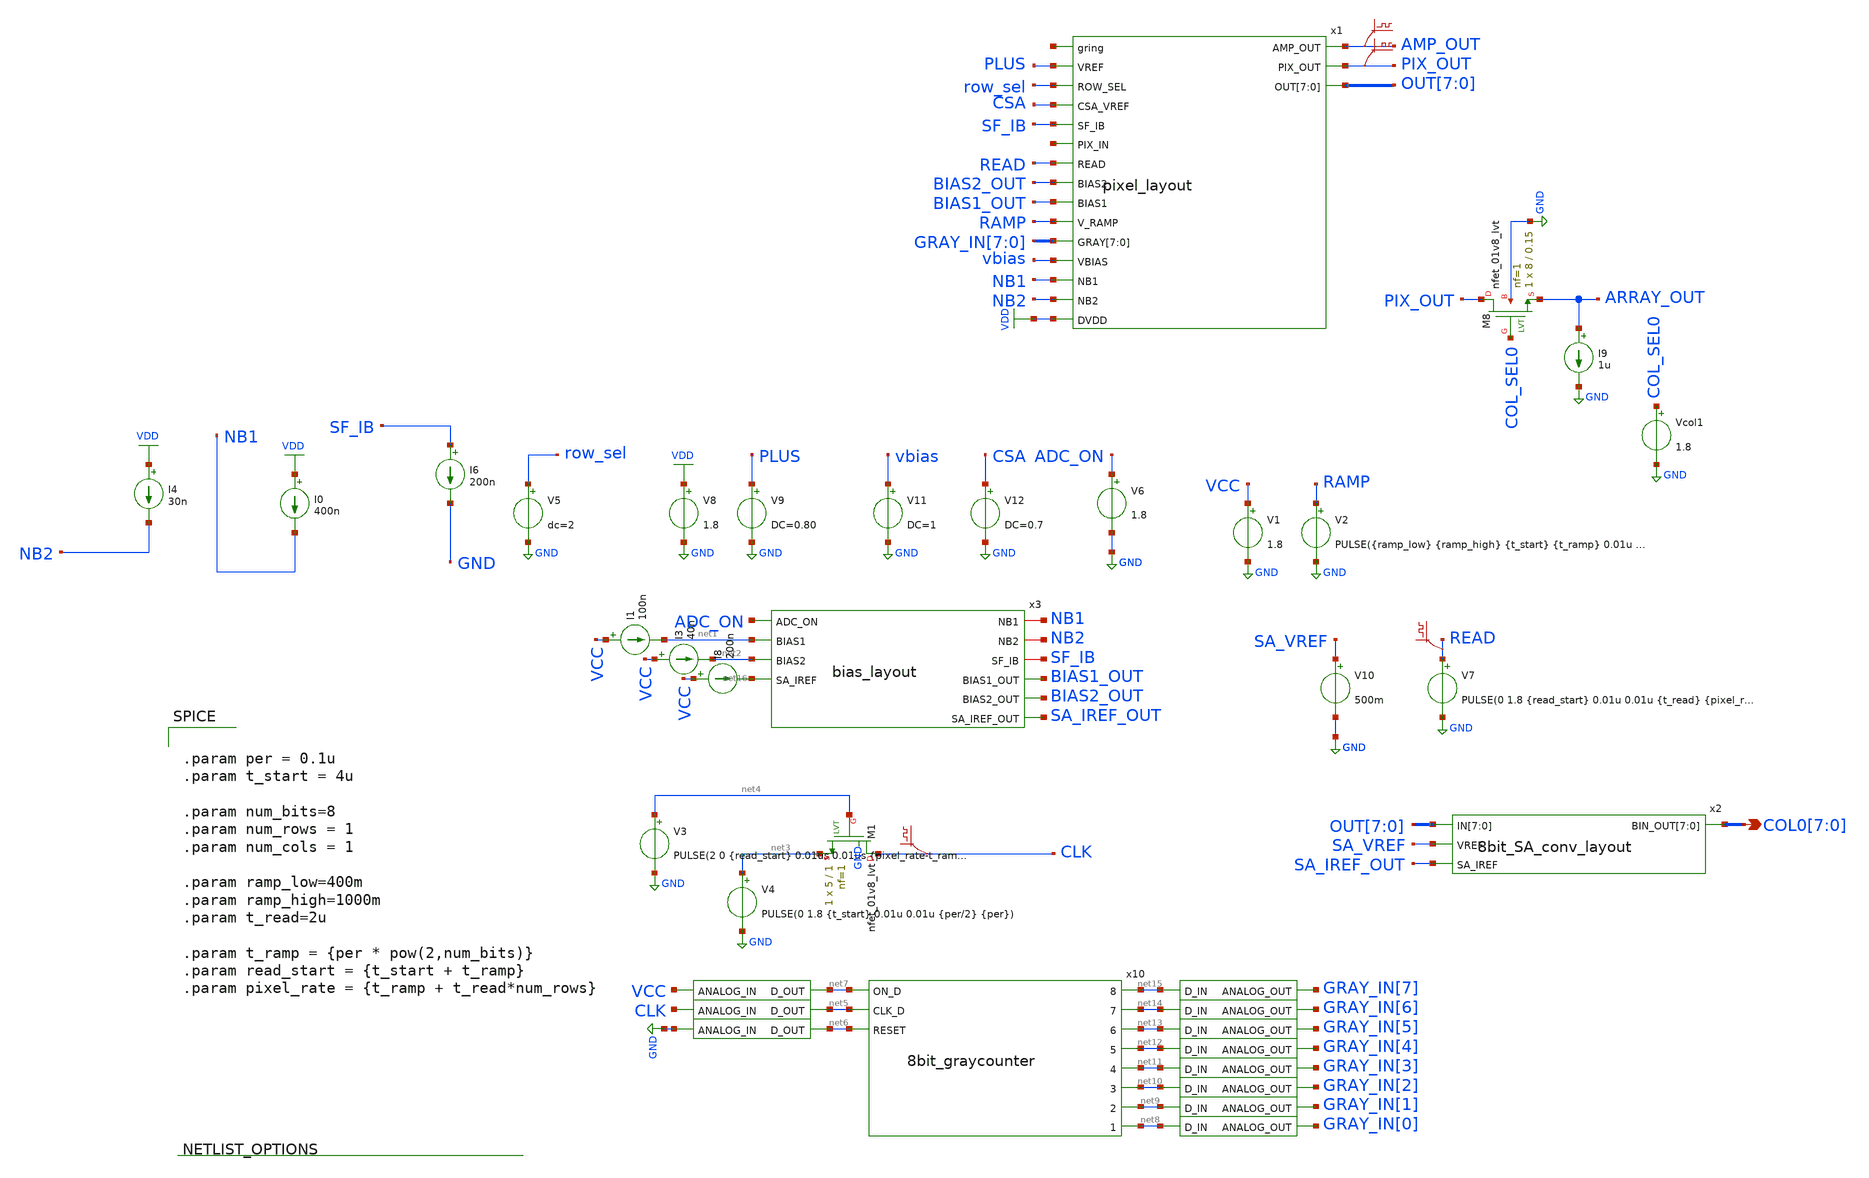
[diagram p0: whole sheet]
** sch_path: xschem/testbench/pixel_components_tb.sch
**.subckt pixel_components_tb COL0[7],COL0[6],COL0[5],COL0[4],COL0[3],COL0[2],COL0[1],COL0[0]
*.opin COL0[7],COL0[6],COL0[5],COL0[4],COL0[3],COL0[2],COL0[1],COL0[0]
V8 VDD GND 1.8
V9 PLUS GND DC=0.80
V11 vbias GND DC=1
V12 CSA GND DC=0.7
I1 VCC net1 100n
I3 VCC net2 40n
I8 VCC net16 200n
V6 ADC_ON GND 1.8
I4 VDD NB2 30n
I6 SF_IB GND 200n
V5 row_sel GND dc=2
I0 VDD NB1 400n
V1 VCC GND 1.8
V2 RAMP GND PULSE({ramp_low} {ramp_high} {t_start} {t_ramp} 0.01u {pixel_rate-t_ramp} {pixel_rate})
V10 SA_VREF GND 500m
V4 net3 GND PULSE(0 1.8 {t_start} 0.01u 0.01u {per/2} {per})
V3 net4 GND PULSE(2 0 {read_start} 0.01us 0.01us {pixel_rate-t_ramp} {pixel_rate})
.save v(clk)
XM1 CLK net4 net3 GND sky130_fd_pr__nfet_01v8_lvt L=1 W=5 nf=1 ad='int((nf+1)/2) * W/nf * 0.29' as='int((nf+2)/2) * W/nf * 0.29'
+ pd='2*int((nf+1)/2) * (W/nf + 0.29)' ps='2*int((nf+2)/2) * (W/nf + 0.29)' nrd='0.29 / W' nrs='0.29 / W'
+ sa=0 sb=0 sd=0 mult=1 m=1
x6 net6 GND adc_bridge
x8 net7 VCC adc_bridge
x7 net5 CLK adc_bridge
x10 net15 net7 net14 net5 net13 net12 net6 net11 net10 net9 net8 8bit_graycounter
x5 GRAY_IN[7] net15 dac_bridge
x9 GRAY_IN[6] net14 dac_bridge
x11 GRAY_IN[5] net13 dac_bridge
x12 GRAY_IN[4] net12 dac_bridge
x13 GRAY_IN[3] net11 dac_bridge
x14 GRAY_IN[2] net10 dac_bridge
x15 GRAY_IN[1] net9 dac_bridge
x16 GRAY_IN[0] net8 dac_bridge
V7 READ GND PULSE(0 1.8 {read_start} 0.01u 0.01u {t_read} {pixel_rate})
.save v(read)
.save v(amp_out)
.save v(pix_out)
XM8 PIX_OUT COL_SEL0 ARRAY_OUT GND sky130_fd_pr__nfet_01v8_lvt L=0.15 W=8 nf=1 ad='int((nf+1)/2) * W/nf * 0.29'
+ as='int((nf+2)/2) * W/nf * 0.29' pd='2*int((nf+1)/2) * (W/nf + 0.29)' ps='2*int((nf+2)/2) * (W/nf + 0.29)'
+ nrd='0.29 / W' nrs='0.29 / W' sa=0 sb=0 sd=0 mult=1 m=1
I9 ARRAY_OUT GND 1u
Vcol1 COL_SEL0 GND 1.8
x1 AMP_OUT net17 PLUS row_sel PIX_OUT CSA OUT[7] OUT[6] OUT[5] OUT[4] OUT[3] OUT[2] OUT[1] OUT[0]
+ SF_IB net18 READ BIAS2_OUT BIAS1_OUT RAMP GRAY_IN[7] GRAY_IN[6] GRAY_IN[5] GRAY_IN[4] GRAY_IN[3]
+ GRAY_IN[2] GRAY_IN[1] GRAY_IN[0] vbias NB1 NB2 VDD pixel_layout
x3 NB1 NB2 SF_IB ADC_ON net1 BIAS1_OUT BIAS2_OUT net2 SA_IREF_OUT net16 bias_layout
x2 OUT[7] OUT[6] OUT[5] OUT[4] OUT[3] OUT[2] OUT[1] OUT[0] SA_VREF SA_IREF_OUT COL0[7] COL0[6]
+ COL0[5] COL0[4] COL0[3] COL0[2] COL0[1] COL0[0] 8bit_SA_conv_layout
**** begin user architecture code

** opencircuitdesign pdks install
.lib $::SKYWATER_MODELS/sky130.lib.spice tt
.global vcc



.param per = 0.1u
.param t_start = 4u

.param num_bits=8
.param num_rows = 1
.param num_cols = 1

.param ramp_low=400m
.param ramp_high=1000m
.param t_read=2u

.param t_ramp = {per * pow(2,num_bits)}
.param read_start = {t_start + t_ramp}
.param pixel_rate = {t_ramp + t_read*num_rows}


**** end user architecture code
**.ends

* expanding   symbol:  digital_prims/adc_bridge.sym # of pins=2
** sym_path: xschem/digital_prims/adc_bridge.sym
** sch_path: xschem/digital_prims/adc_bridge.sch
.subckt adc_bridge D_OUT ANALOG_IN
*.ipin ANALOG_IN
*.opin D_OUT
**** begin user architecture code


abridge [ANALOG_IN] [D_OUT] adc_buff
.model adc_buff adc_bridge(in_low=0.9 in_high =0.9)


**** end user architecture code
.ends


* expanding   symbol:  adc/8bit_graycounter.sym # of pins=11
** sym_path: xschem/adc/8bit_graycounter.sym
** sch_path: xschem/adc/8bit_graycounter.sch
.subckt 8bit_graycounter 8 ON_D 7 CLK_D 6 5 RESET 4 3 2 1
*.ipin ON_D
*.ipin CLK_D
*.ipin RESET
*.opin 7
*.opin 6
*.opin 5
*.opin 4
*.opin 3
*.opin 2
*.opin 1
*.opin 8
**** begin user architecture code


a1 [ON_D] CLK_D RESET [8 7 6 5 4 3 2 1] gc_sm
.model gc_sm d_state(state_file="/home/hni/topmetal_dps/xschem/adc/graycntr.in")


**** end user architecture code
.ends


* expanding   symbol:  digital_prims/dac_bridge.sym # of pins=2
** sym_path: xschem/digital_prims/dac_bridge.sym
** sch_path: xschem/digital_prims/dac_bridge.sch
.subckt dac_bridge ANALOG_OUT D_IN
*.ipin D_IN
*.opin ANALOG_OUT
**** begin user architecture code


abridge_d [D_IN] [ANALOG_OUT] dac_buff
.model dac_buff dac_bridge(out_high=1.8)


**** end user architecture code
.ends


* expanding   symbol:  post_layout/pixel_layout.sym # of pins=18
** sym_path: xschem/post_layout/pixel_layout.sym
** sch_path: xschem/post_layout/pixel_layout.sch
.subckt pixel_layout AMP_OUT gring VREF ROW_SEL PIX_OUT CSA_VREF OUT[7] OUT[6] OUT[5] OUT[4] OUT[3]
+ OUT[2] OUT[1] OUT[0] SF_IB PIX_IN READ BIAS2 BIAS1 V_RAMP GRAY[7] GRAY[6] GRAY[5] GRAY[4] GRAY[3] GRAY[2]
+ GRAY[1] GRAY[0] VBIAS NB1 NB2 DVDD
*.opin AMP_OUT
*.ipin gring
*.ipin VREF
*.ipin ROW_SEL
*.opin PIX_OUT
*.ipin CSA_VREF
*.ipin SF_IB
*.ipin PIX_IN
*.ipin READ
*.ipin BIAS2
*.ipin BIAS1
*.ipin V_RAMP
*.ipin GRAY[7],GRAY[6],GRAY[5],GRAY[4],GRAY[3],GRAY[2],GRAY[1],GRAY[0]
*.ipin VBIAS
*.ipin NB1
*.ipin NB2
*.ipin DVDD
*.opin OUT[7],OUT[6],OUT[5],OUT[4],OUT[3],OUT[2],OUT[1],OUT[0]
**** begin user architecture code


X8bit_dram_0 READ GRAYx2x OUTx4x OUTx2x OUTx6x GRAYx3x GRAYx4x OUTx0x GRAYx1x OUTx7x  GRAYx5x OUTx3x
+ GRAYx7x 8bit_dram_0/4bit_dram_1/dram_array_1/dram_cell_1/WWL OUTx5x  OUTx1x GRAYx6x GND GRAYx0x x8bit_dram
X0 a_2200_n380# ROW_SEL PIX_OUT GND sky130_fd_pr__nfet_01v8_lvt ad=6.5e+11p pd=5e+06u as=1e+12p
+ ps=5e+06u w=2e+06u l=1e+06u
X1 DVDD a_1000_n1450# a_1000_n1450# DVDD sky130_fd_pr__pfet_01v8_lvt ad=1.45e+12p pd=1.09e+07u
+ as=3.5e+11p ps=2.7e+06u w=1e+06u l=1e+06u
X2 8bit_dram_0/4bit_dram_1/dram_array_1/dram_cell_1/WWL a_1870_n1400# GND GND
+ sky130_fd_pr__nfet_01v8 ad=4e+11p pd=2.8e+06u as=8.70025e+11p ps=7.105e+06u w=1e+06u l=150000u
X3 GND NB1 a_n30_n2640# GND sky130_fd_pr__nfet_01v8_lvt ad=0p pd=0u as=3.22e+12p ps=1.79e+07u
+ w=1.2e+06u l=1e+06u
X4 a_n140_n550# VBIAS a_n140_n780# GND sky130_fd_pr__nfet_01v8_lvt ad=3.5e+11p pd=2.7e+06u
+ as=2.1525e+12p ps=1.76e+07u w=1e+06u l=800000u
X5 a_1720_n1450# V_RAMP a_1100_n1450# GND sky130_fd_pr__nfet_01v8_lvt ad=3.5e+11p pd=2.7e+06u
+ as=8.8e+11p ps=7.1e+06u w=1e+06u l=150000u
X6 a_1870_n1400# a_1720_n1450# DVDD DVDD sky130_fd_pr__pfet_01v8_lvt ad=3.5e+11p pd=2.7e+06u as=0p
+ ps=0u w=1e+06u l=450000u
X7 a_1100_n1450# AMP_OUT a_1000_n1450# GND sky130_fd_pr__nfet_01v8_lvt ad=0p pd=0u as=3.5e+11p
+ ps=2.7e+06u w=1e+06u l=150000u
X8 a_2287_n292# AMP_OUT GND VDD sky130_fd_pr__pfet_01v8_lvt ad=5e+11p pd=3e+06u as=3.50025e+11p
+ ps=2.705e+06u w=1e+06u l=1e+06u
X9 8bit_dram_0/4bit_dram_1/dram_array_1/dram_cell_1/WWL a_1870_n1400# DVDD DVDD
+ sky130_fd_pr__pfet_01v8 ad=3.5e+11p pd=2.7e+06u as=0p ps=0u w=1e+06u l=200000u
X10 AMP_OUT NB2 GND GND sky130_fd_pr__nfet_01v8_lvt ad=6.975e+11p pd=5.7e+06u as=0p ps=0u w=1e+06u
+ l=1.2e+06u
X11 a_1100_n1450# BIAS1 GND GND sky130_fd_pr__nfet_01v8 ad=0p pd=0u as=0p ps=0u w=450000u l=1e+06u
X12 a_350_10# a_n140_n550# a_n140_n550# VDD sky130_fd_pr__pfet_01v8_lvt ad=3.5e+11p pd=2.7e+06u
+ as=3.5e+11p ps=2.7e+06u w=1e+06u l=2e+06u
X13 VDD SF_IB a_2287_n292# VDD sky130_fd_pr__pfet_01v8_lvt ad=1.05e+12p pd=8.1e+06u as=0p ps=0u
+ w=1e+06u l=1e+06u
X14 PIX_IN AMP_OUT sky130_fd_pr__cap_mim_m3_1 l=2e+06u w=2e+06u
X15 a_n30_n2640# VREF a_n140_n780# GND sky130_fd_pr__nfet_01v8_lvt ad=0p pd=0u as=0p ps=0u w=7e+06u
+ l=150000u
X16 VDD a_350_10# a_350_10# VDD sky130_fd_pr__pfet_01v8_lvt ad=0p pd=0u as=0p ps=0u w=1e+06u
+ l=2e+06u
X17 a_1460_10# a_350_10# VDD VDD sky130_fd_pr__pfet_01v8_lvt ad=3.5e+11p pd=2.7e+06u as=0p ps=0u
+ w=1e+06u l=2e+06u
X18 AMP_OUT CSA_VREF PIX_IN VDD sky130_fd_pr__pfet_01v8_lvt ad=2.94e+11p pd=2.24e+06u as=2.73e+11p
+ ps=2.14e+06u w=420000u l=8e+06u
X19 a_1870_n1400# BIAS2 GND GND sky130_fd_pr__nfet_01v8_lvt ad=3.5e+11p pd=2.7e+06u as=0p ps=0u
+ w=1e+06u l=1e+06u
X20 a_120_n550# a_n140_n550# a_1460_10# VDD sky130_fd_pr__pfet_01v8_lvt ad=3.5e+11p pd=2.7e+06u
+ as=0p ps=0u w=1e+06u l=2e+06u
X21 a_120_n550# VBIAS a_120_n780# GND sky130_fd_pr__nfet_01v8_lvt ad=3.5e+11p pd=2.7e+06u
+ as=2.1525e+12p ps=1.76e+07u w=1e+06u l=800000u
X22 a_120_n780# PIX_IN a_n30_n2640# GND sky130_fd_pr__nfet_01v8_lvt ad=0p pd=0u as=0p ps=0u w=7e+06u
+ l=150000u
X23 a_1720_n1450# a_1000_n1450# DVDD DVDD sky130_fd_pr__pfet_01v8_lvt ad=3.5e+11p pd=2.7e+06u as=0p
+ ps=0u w=1e+06u l=1e+06u
X24 VDD a_120_n550# AMP_OUT GND sky130_fd_pr__nfet_01v8_lvt ad=1.185e+12p pd=8.4e+06u as=0p ps=0u
+ w=1e+06u l=1e+06u
X25 VDD a_2287_n292# a_2200_n380# GND sky130_fd_pr__nfet_01v8_lvt ad=0p pd=0u as=0p ps=0u w=1e+06u
+ l=150000u



.subckt dram_cell storage WWL WBL RWL RBL VSUBS
X0 RWL storage RBL VSUBS sky130_fd_pr__nfet_01v8 ad=3e+11p pd=2.6e+06u as=3.5e+11p ps=2.7e+06u
+ w=1e+06u l=150000u
X1 storage WWL WBL VSUBS sky130_fd_pr__nfet_01v8 ad=3.5e+11p pd=2.7e+06u as=3e+11p ps=2.6e+06u
+ w=1e+06u l=150000u
.ends

.subckt dram_array dram_cell_1/WWL dram_cell_1/RWL dram_cell_0/WBL dram_cell_1/WBL  dram_cell_1/RBL
+ dram_cell_0/RBL VSUBS dram_cell_0/RWL
Xdram_cell_0 dram_cell_0/storage dram_cell_1/WWL dram_cell_0/WBL dram_cell_0/RWL dram_cell_0/RBL
+  VSUBS dram_cell
Xdram_cell_1 dram_cell_1/storage dram_cell_1/WWL dram_cell_1/WBL dram_cell_1/RWL dram_cell_1/RBL
+  VSUBS dram_cell
.ends

.subckt x4bit_dram dram_array_1/dram_cell_0/RWL dram_array_1/dram_cell_0/WBL
+ dram_array_1/dram_cell_1/RWL  dram_array_1/dram_cell_0/RBL dram_array_0/dram_cell_0/RBL dram_array_0/dram_cell_1/WBL
+  dram_array_1/dram_cell_1/WBL dram_array_0/dram_cell_1/RBL dram_array_1/dram_cell_1/RBL  dram_array_0/dram_cell_0/WBL
+ dram_array_1/dram_cell_1/WWL VSUBS
Xdram_array_0 dram_array_1/dram_cell_1/WWL dram_array_1/dram_cell_0/RWL dram_array_0/dram_cell_0/WBL
+  dram_array_0/dram_cell_1/WBL dram_array_0/dram_cell_1/RBL dram_array_0/dram_cell_0/RBL  VSUBS dram_array_1/dram_cell_0/RWL
+ dram_array
Xdram_array_1 dram_array_1/dram_cell_1/WWL dram_array_1/dram_cell_1/RWL dram_array_1/dram_cell_0/WBL
+  dram_array_1/dram_cell_1/WBL dram_array_1/dram_cell_1/RBL dram_array_1/dram_cell_0/RBL  VSUBS dram_array_1/dram_cell_0/RWL
+ dram_array
.ends

.subckt x8bit_dram 4bit_dram_1/dram_array_1/dram_cell_1/RWL 4bit_dram_0/dram_array_1/dram_cell_0/WBL
+  4bit_dram_1/dram_array_0/dram_cell_0/RBL 4bit_dram_0/dram_array_1/dram_cell_0/RBL  4bit_dram_1/dram_array_1/dram_cell_0/RBL
+ 4bit_dram_0/dram_array_1/dram_cell_1/WBL  4bit_dram_1/dram_array_0/dram_cell_0/WBL 4bit_dram_0/dram_array_0/dram_cell_0/RBL
+  4bit_dram_0/dram_array_0/dram_cell_1/WBL 4bit_dram_1/dram_array_1/dram_cell_1/RBL  4bit_dram_1/dram_array_0/dram_cell_1/WBL
+ 4bit_dram_0/dram_array_1/dram_cell_1/RBL  4bit_dram_1/dram_array_1/dram_cell_1/WBL 4bit_dram_1/dram_array_1/dram_cell_1/WWL
+  4bit_dram_1/dram_array_0/dram_cell_1/RBL 4bit_dram_0/dram_array_0/dram_cell_1/RBL  4bit_dram_1/dram_array_1/dram_cell_0/WBL VSUBS
+ 4bit_dram_0/dram_array_0/dram_cell_0/WBL
X4bit_dram_1 4bit_dram_1/dram_array_1/dram_cell_1/RWL 4bit_dram_1/dram_array_1/dram_cell_0/WBL
+  4bit_dram_1/dram_array_1/dram_cell_1/RWL 4bit_dram_1/dram_array_1/dram_cell_0/RBL  4bit_dram_1/dram_array_0/dram_cell_0/RBL
+ 4bit_dram_1/dram_array_0/dram_cell_1/WBL  4bit_dram_1/dram_array_1/dram_cell_1/WBL 4bit_dram_1/dram_array_0/dram_cell_1/RBL
+  4bit_dram_1/dram_array_1/dram_cell_1/RBL 4bit_dram_1/dram_array_0/dram_cell_0/WBL  4bit_dram_1/dram_array_1/dram_cell_1/WWL VSUBS x4bit_dram
X4bit_dram_0 4bit_dram_1/dram_array_1/dram_cell_1/RWL 4bit_dram_0/dram_array_1/dram_cell_0/WBL
+  4bit_dram_1/dram_array_1/dram_cell_1/RWL 4bit_dram_0/dram_array_1/dram_cell_0/RBL  4bit_dram_0/dram_array_0/dram_cell_0/RBL
+ 4bit_dram_0/dram_array_0/dram_cell_1/WBL  4bit_dram_0/dram_array_1/dram_cell_1/WBL 4bit_dram_0/dram_array_0/dram_cell_1/RBL
+  4bit_dram_0/dram_array_1/dram_cell_1/RBL 4bit_dram_0/dram_array_0/dram_cell_0/WBL  4bit_dram_1/dram_array_1/dram_cell_1/WWL VSUBS x4bit_dram
.ends




**** end user architecture code
.ends


* expanding   symbol:  post_layout/bias_layout.sym # of pins=10
** sym_path: xschem/post_layout/bias_layout.sym
** sch_path: xschem/post_layout/bias_layout.sch
.subckt bias_layout NB1 NB2 SF_IB ADC_ON BIAS1 BIAS1_OUT BIAS2_OUT BIAS2 SA_IREF_OUT SA_IREF
*.iopin SF_IB
*.iopin NB2
*.ipin ADC_ON
*.ipin BIAS1
*.opin BIAS1_OUT
*.ipin BIAS2
*.opin BIAS2_OUT
*.ipin SA_IREF
*.opin SA_IREF_OUT
*.iopin NB1
**** begin user architecture code


X0 BIAS1 ADC_ON BIAS1_OUT GND sky130_fd_pr__nfet_01v8 ad=2.5e+12p pd=1.1e+07u as=5.9425e+12p
+ ps=1.514e+07u w=5e+06u l=1e+06u
X1 NB1 NB1 GND GND sky130_fd_pr__nfet_01v8_lvt ad=3.5e+11p pd=2.7e+06u as=1.272e+13p ps=4.894e+07u
+ w=1e+06u l=1.2e+06u
X2 BIAS2_OUT BIAS2_OUT GND GND sky130_fd_pr__nfet_01v8_lvt ad=5.9725e+12p pd=1.52e+07u as=0p ps=0u
+ w=1e+06u l=1e+06u
X3 SA_IREF_OUT SA_IREF_OUT GND GND sky130_fd_pr__nfet_01v8 ad=5.9905e+12p pd=1.53e+07u as=0p ps=0u
+ w=500000u l=1e+06u
X4 NB2 NB2 GND GND sky130_fd_pr__nfet_01v8_lvt ad=3.5e+11p pd=2.7e+06u as=0p ps=0u w=1e+06u
+ l=1.2e+06u
X5 BIAS2 ADC_ON BIAS2_OUT GND sky130_fd_pr__nfet_01v8 ad=2.5e+12p pd=1.1e+07u as=0p ps=0u w=5e+06u
+ l=1e+06u
X6 AMP_IB AMP_IB GND GND sky130_fd_pr__nfet_01v8_lvt ad=5.6e+12p pd=1.74e+07u as=0p ps=0u w=8e+06u
+ l=2e+06u
X7 OUT_IB OUT_IB GND GND sky130_fd_pr__nfet_01v8_lvt ad=5.6e+12p pd=1.74e+07u as=0p ps=0u w=8e+06u
+ l=2e+06u
X8 SA_IREF ADC_ON SA_IREF_OUT GND sky130_fd_pr__nfet_01v8 ad=2.5e+12p pd=1.1e+07u as=0p ps=0u
+ w=5e+06u l=1e+06u
X9 BIAS1_OUT BIAS1_OUT GND GND sky130_fd_pr__nfet_01v8 ad=0p pd=0u as=0p ps=0u w=420000u l=1e+06u
X10 SF_IB SF_IB VDD VDD sky130_fd_pr__pfet_01v8_lvt ad=5.5e+11p pd=3.1e+06u as=4.5e+11p ps=2.9e+06u
+ w=1e+06u l=1e+06u




**** end user architecture code
.ends


* expanding   symbol:  post_layout/8bit_SA_conv_layout.sym # of pins=4
** sym_path: xschem/post_layout/8bit_SA_conv_layout.sym
** sch_path: xschem/post_layout/8bit_SA_conv_layout.sch
.subckt 8bit_SA_conv_layout IN[7] IN[6] IN[5] IN[4] IN[3] IN[2] IN[1] IN[0] VREF SA_IREF BIN_OUT[7]
+ BIN_OUT[6] BIN_OUT[5] BIN_OUT[4] BIN_OUT[3] BIN_OUT[2] BIN_OUT[1] BIN_OUT[0]
*.ipin IN[7],IN[6],IN[5],IN[4],IN[3],IN[2],IN[1],IN[0]
*.ipin VREF
*.opin BIN_OUT[7],BIN_OUT[6],BIN_OUT[5],BIN_OUT[4],BIN_OUT[3],BIN_OUT[2],BIN_OUT[1],BIN_OUT[0]
*.ipin SA_IREF
x11 net8 net9 net10 net7 net6 net11 net5 net12 net13 net4 net3 net14 net15 net2 net16 net1
+ 8bitgray2bin
x12 BIN_OUT[7] net8 dac_bridge
x13 BIN_OUT[6] net7 dac_bridge
x14 BIN_OUT[5] net6 dac_bridge
x16 BIN_OUT[4] net5 dac_bridge
x17 BIN_OUT[3] net4 dac_bridge
x18 BIN_OUT[2] net3 dac_bridge
x19 BIN_OUT[1] net2 dac_bridge
x37 BIN_OUT[0] net1 dac_bridge
x39 net9 OUT_A[7] adc_bridge
x40 net10 OUT_A[6] adc_bridge
x41 net11 OUT_A[5] adc_bridge
x42 net12 OUT_A[4] adc_bridge
x43 net13 OUT_A[3] adc_bridge
x44 net14 OUT_A[2] adc_bridge
x45 net15 OUT_A[1] adc_bridge
x46 net16 OUT_A[0] adc_bridge
.save v(bin_out[7])
.save v(bin_out[6])
.save v(bin_out[5])
.save v(bin_out[4])
.save v(bin_out[3])
.save v(bin_out[2])
.save v(bin_out[1])
.save v(bin_out[0])
**** begin user architecture code


Xsens_amp_2 INx5x SA_IREF OUT_Ax5x VREF VDD GND sens_amp
Xsens_amp_3 INx4x SA_IREF OUT_Ax4x VREF VDD GND sens_amp
Xsens_amp_4 INx3x SA_IREF OUT_Ax3x VREF VDD GND sens_amp
Xsens_amp_5 INx2x SA_IREF OUT_Ax2x VREF VDD GND sens_amp
Xsens_amp_6 INx1x SA_IREF OUT_Ax1x VREF VDD GND sens_amp
Xsens_amp_7 INx0x SA_IREF OUT_Ax0x VREF VDD GND sens_amp
Xsens_amp_0 INx7x SA_IREF OUT_Ax7x VREF VDD GND sens_amp
Xsens_amp_1 INx6x SA_IREF OUT_Ax6x VREF VDD GND sens_amp


.subckt sens_amp V_IN SA_IREF OUT REF VDD GND
X0 GN GN VDD VDD sky130_fd_pr__pfet_01v8_lvt ad=3.5e+11p pd=2.7e+06u as=1.8e+12p ps=1.22e+07u
+ w=1e+06u l=500000u
X1 net1 V_IN net2 GND sky130_fd_pr__nfet_01v8_lvt ad=1.4e+12p pd=8.7e+06u as=1.775e+12p ps=1.05e+07u
+ w=4e+06u l=150000u
X2 net2 REF GN GND sky130_fd_pr__nfet_01v8_lvt ad=0p pd=0u as=1.45e+12p ps=9.1e+06u w=4e+06u
+ l=150000u
X3 net1 GN VDD VDD sky130_fd_pr__pfet_01v8_lvt ad=3.5e+11p pd=2.7e+06u as=0p ps=0u w=1e+06u
+ l=500000u
X4 net2 SA_IREF GND GND sky130_fd_pr__nfet_01v8_lvt ad=0p pd=0u as=6e+11p ps=4.7e+06u w=500000u
+ l=1e+06u
X5 OUT net1 VDD VDD sky130_fd_pr__pfet_01v8_lvt ad=1.05e+12p pd=6.7e+06u as=0p ps=0u w=3e+06u
+ l=350000u
X6 OUT net1 GND GND sky130_fd_pr__nfet_01v8_lvt ad=3.5e+11p pd=2.7e+06u as=0p ps=0u w=1e+06u
+ l=150000u
.ends




**** end user architecture code
.ends


* expanding   symbol:  adc/8bitgray2bin.sym # of pins=16
** sym_path: xschem/adc/8bitgray2bin.sym
** sch_path: xschem/adc/8bitgray2bin.sch
.subckt 8bitgray2bin 8 g8 g7 7 6 g6 5 g5 g4 4 3 g3 g2 2 g1 1
*.opin 7
*.opin 6
*.opin 5
*.opin 4
*.opin 3
*.opin 2
*.opin 1
*.opin 8
*.ipin g5
*.ipin g4
*.ipin g3
*.ipin g8
*.ipin g7
*.ipin g6
*.ipin g2
*.ipin g1
**** begin user architecture code


* lsb first.
a1 [g1 g2 g3 g4 g5 g6 g7 g8] [1 2 3 4 5 6 7 8] gray2bin_lut
.model gray2bin_lut d_genlut(rise_delay=[1p 1p] fall_delay=[1p 1p]  input_load=[1p 1p]
+ input_delay=[0 0]
+ table_values=01101001100101101001011001101001100101100110100101101001100101101001011001101001011010011001011001101001100101101001011001101001100101100110100101101001100101100110100110010110100101100110100101101001100101101001011001101001100101100110100101101001100101100011110011000011110000110011110011000011001111000011110011000011110000110011110000111100110000110011110011000011110000110011110011000011001111000011110011000011001111001100001111000011001111000011110011000011110000110011110011000011001111000011110011000011000011111111000011110000000011111111000000001111000011111111000011110000000011110000111111110000000011111111000011110000000011111111000000001111000011111111000000001111111100001111000000001111000011111111000011110000000011111111000000001111000011111111000000000000111111111111111100000000111111110000000000000000111111111111111100000000000000001111111100000000111111111111111100000000111111110000000000000000111111110000000011111111111111110000000000000000111111111111111100000000111111110000000000000000111111110000000000000000111111111111111111111111111111110000000000000000111111111111111100000000000000000000000000000000111111111111111111111111111111110000000000000000000000000000000011111111111111110000000000000000111111111111111111111111111111110000000000000000000000000000000000000000000000001111111111111111111111111111111111111111111111111111111111111111000000000000000000000000000000001111111111111111111111111111111100000000000000000000000000000000000000000000000000000000000000001111111111111111111111111111111100000000000000000000000000000000000000000000000000000000000000001111111111111111111111111111111111111111111111111111111111111111111111111111111111111111111111111111111111111111111111111111111100000000000000000000000000000000000000000000000000000000000000000000000000000000000000000000000000000000000000000000000000000000000000000000000000000000000000000000000000000000000000000000000011111111111111111111111111111111111111111111111111111111111111111111111111111111111111111111111111111111111111111111111111111111)




**** end user architecture code
.ends

.GLOBAL GND
.GLOBAL VDD
**** begin user architecture code


.options gmin=10e-20
.control
save all

*dc v2 0 1.8 0.05
*plot v(test)
tran 1u 200u

write pixel_components_tb.raw
.endc


**** end user architecture code
.end
